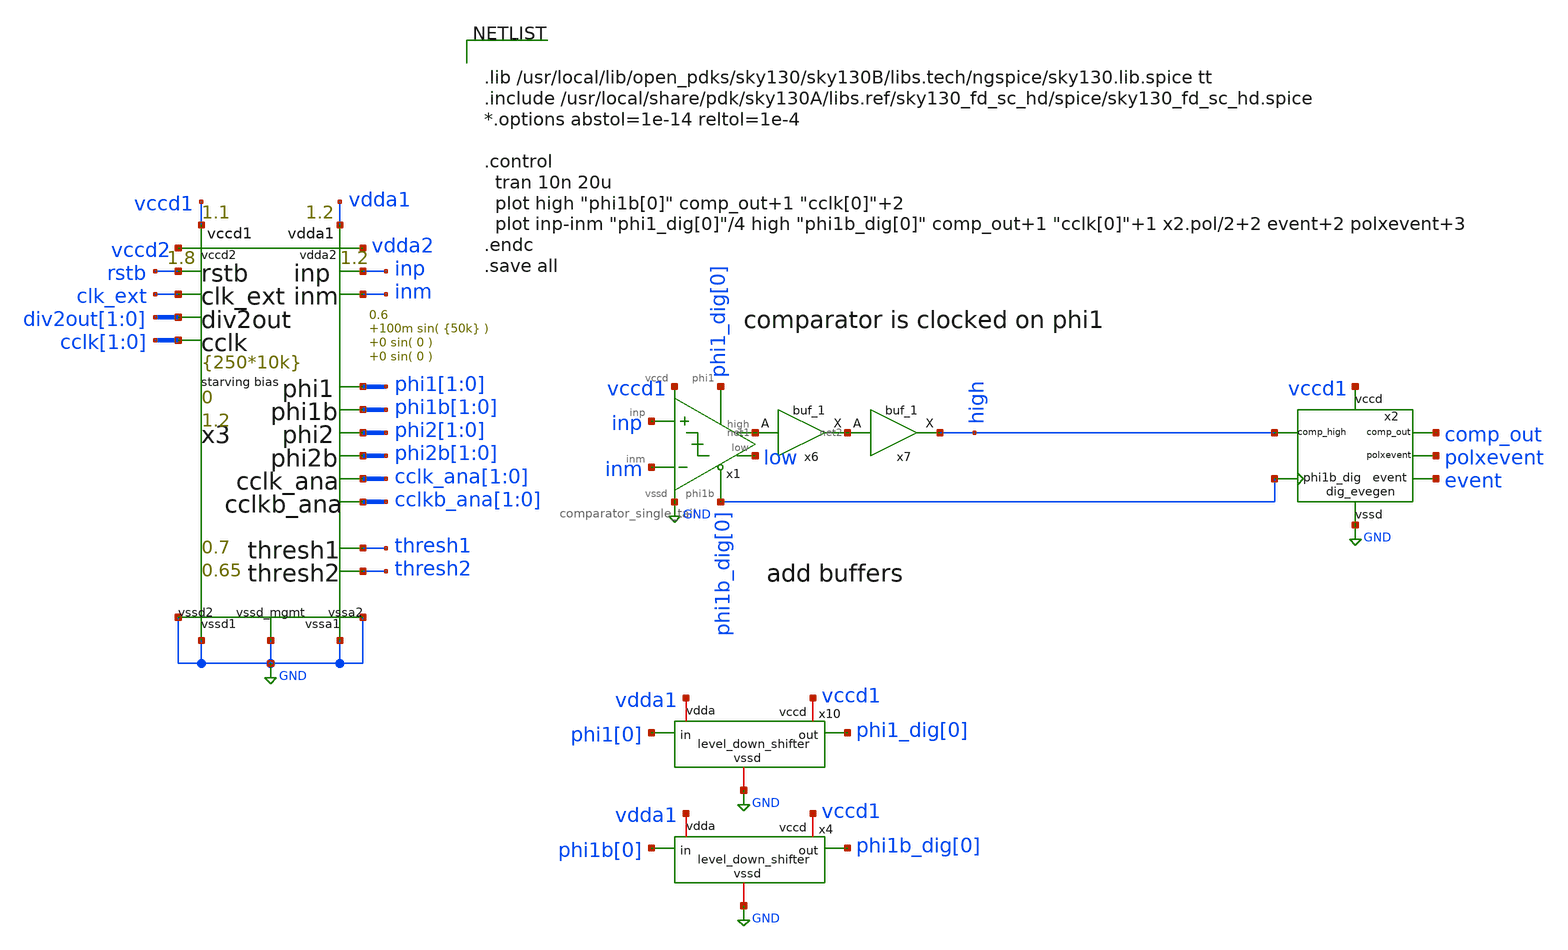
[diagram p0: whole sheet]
** sch_path: xschem/test_bench/comparator_pol_event_tb.sch
**.subckt comparator_pol_event_tb
x1 inp inm net1 phi1_dig[0] phi1b_dig[0] low vccd1 GND comparator_single_tail Wplus=0.42 Lplus=0.42
+ Wminus=0.42 Lminus=0.15
x6 net1 gnd gnd vccd1 vccd1 net2 sky130_fd_sc_hd__buf_1
x7 net2 gnd gnd vccd1 vccd1 high sky130_fd_sc_hd__buf_1
x2 phi1b_dig[0] event polxevent vccd1 GND high comp_out dig_evegen
x10 vdda1 vccd1 phi1[0] phi1_dig[0] GND level_down_shifter
x4 vdda1 vccd1 phi1b[0] phi1b_dig[0] GND level_down_shifter
x3 thresh1 thresh2 inp inm clk_ext rstb phi1[1] phi1[0] phi1b[1] phi1b[0] phi2[1] phi2[0] phi2b[1] phi2b[0]
+ cclk_ana[1] cclk_ana[0] cclkb_ana[1] cclkb_ana[0] div2out[1] div2out[0] cclk[1] cclk[0] vdda1 vccd1 vccd2
+ vdda2 GND GND GND GND GND risc_signals p_vdda1=1.2 p_vdda2=1.2 p_vccd1=1.1 p_vccd2=1.8 p_vccd_mgmt=1.8
+ p_fclk={250*10k} p_duty_cycle=0.5 p_rstb_delay={1.5/p_fclk} p_rstb_tr=5n p_thresh1=0.7 p_thresh2=0.65
+ p_vpb=0 p_vnb=1.2 p_vcm=0.6 p_amp1=100m p_f1={50k} p_amp2=0 p_f2=0 p_amp3=0 p_f3=0
**** begin user architecture code


.lib /usr/local/lib/open_pdks/sky130/sky130B/libs.tech/ngspice/sky130.lib.spice tt
.include /usr/local/share/pdk/sky130A/libs.ref/sky130_fd_sc_hd/spice/sky130_fd_sc_hd.spice
*.options abstol=1e-14 reltol=1e-4

.control
  tran 10n 20u
  plot high "phi1b[0]" comp_out+1 "cclk[0]"+2
  plot inp-inm "phi1_dig[0]"/4 high "phi1b_dig[0]" comp_out+1 "cclk[0]"+1 x2.pol/2+2 event+2
+ polxevent+3
.endc
.save all


**** end user architecture code
**.ends
.GLOBAL GND
.end
